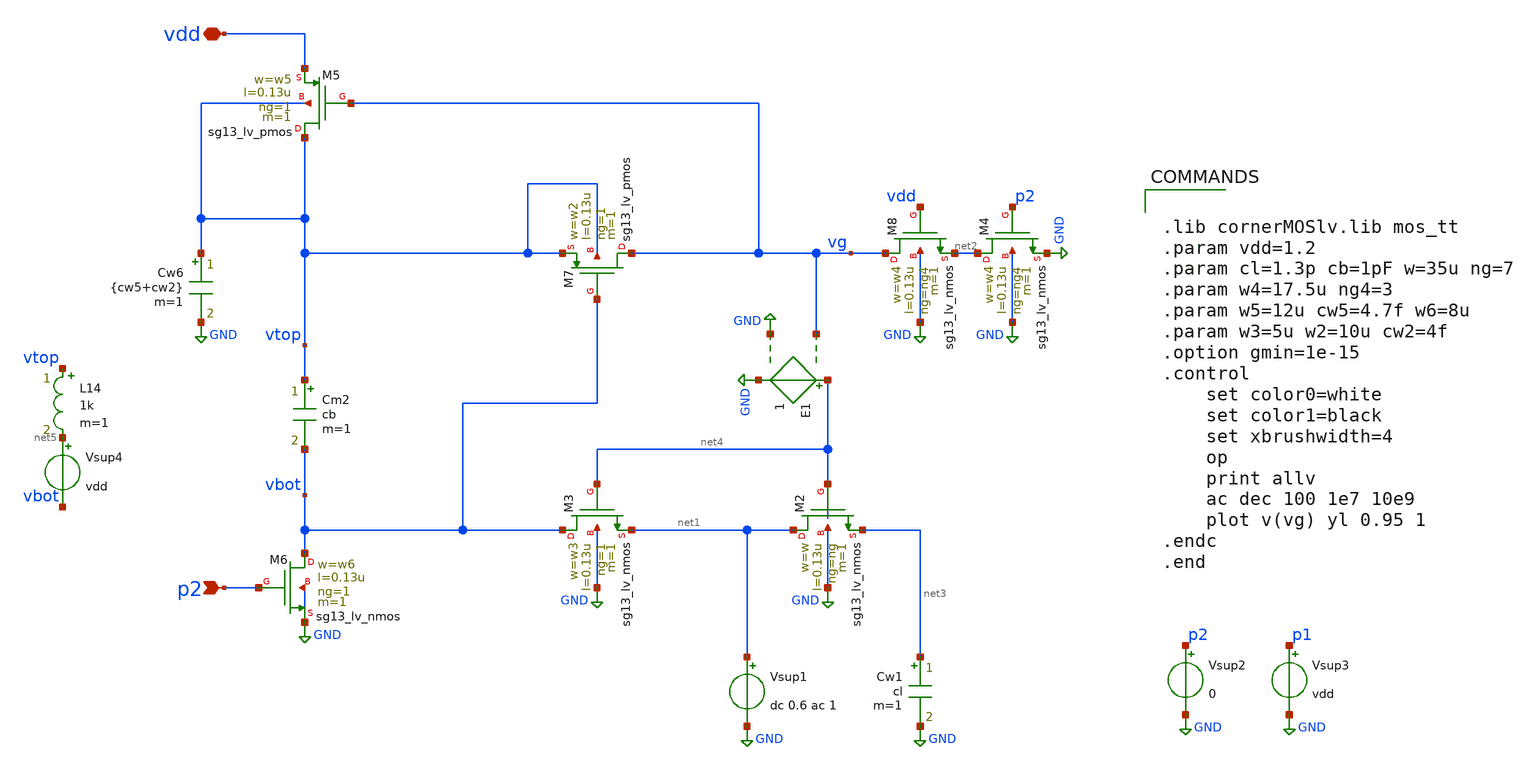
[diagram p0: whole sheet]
** sch_path: xschem/tb_boot4_csmall.sch
**.subckt tb_boot4_csmall p2 vdd
*.ipin p2
*.iopin vdd
Vsup4 net5 vbot vdd
Cm2 vtop vbot cb m=1
XM2 net1 net4 net3 GND sg13_lv_nmos w=w l=0.13u ng=ng m=1 mm_ok=1
XM8 vg vdd net2 GND sg13_lv_nmos w=w4 l=0.13u ng=ng4 m=1 mm_ok=1
XM4 net2 p2 GND GND sg13_lv_nmos w=w4 l=0.13u ng=ng4 m=1 mm_ok=1
XM6 vbot p2 GND GND sg13_lv_nmos w=w6 l=0.13u ng=1 m=1 mm_ok=1
XM5 vtop vg vdd vtop sg13_lv_pmos w=w5 l=0.13u ng=1 m=1 mm_ok=1
Cw6 vtop GND {cw5+cw2} m=1
XM3 vbot net4 net1 GND sg13_lv_nmos w=w3 l=0.13u ng=1 m=1 mm_ok=1
XM7 vg vbot vtop vtop sg13_lv_pmos w=w2 l=0.13u ng=1 m=1 mm_ok=1
Cw1 net3 GND cl m=1
Vsup1 net1 GND dc 0.6 ac 1
Vsup2 p2 GND 0
Vsup3 p1 GND vdd
E1 net4 GND vg GND 1
L14 vtop net5 1k m=1
**** begin user architecture code


.lib cornerMOSlv.lib mos_tt
.param vdd=1.2
.param cl=1.3p cb=1pF w=35u ng=7
.param w4=17.5u ng4=3
.param w5=12u cw5=4.7f w6=8u
.param w3=5u w2=10u cw2=4f
.option gmin=1e-15
.control
    set color0=white
    set color1=black
    set xbrushwidth=4
    op
    print allv
    ac dec 100 1e7 10e9
    plot v(vg) yl 0.95 1
.endc
.end


**** end user architecture code
**.ends
.GLOBAL GND
.end
